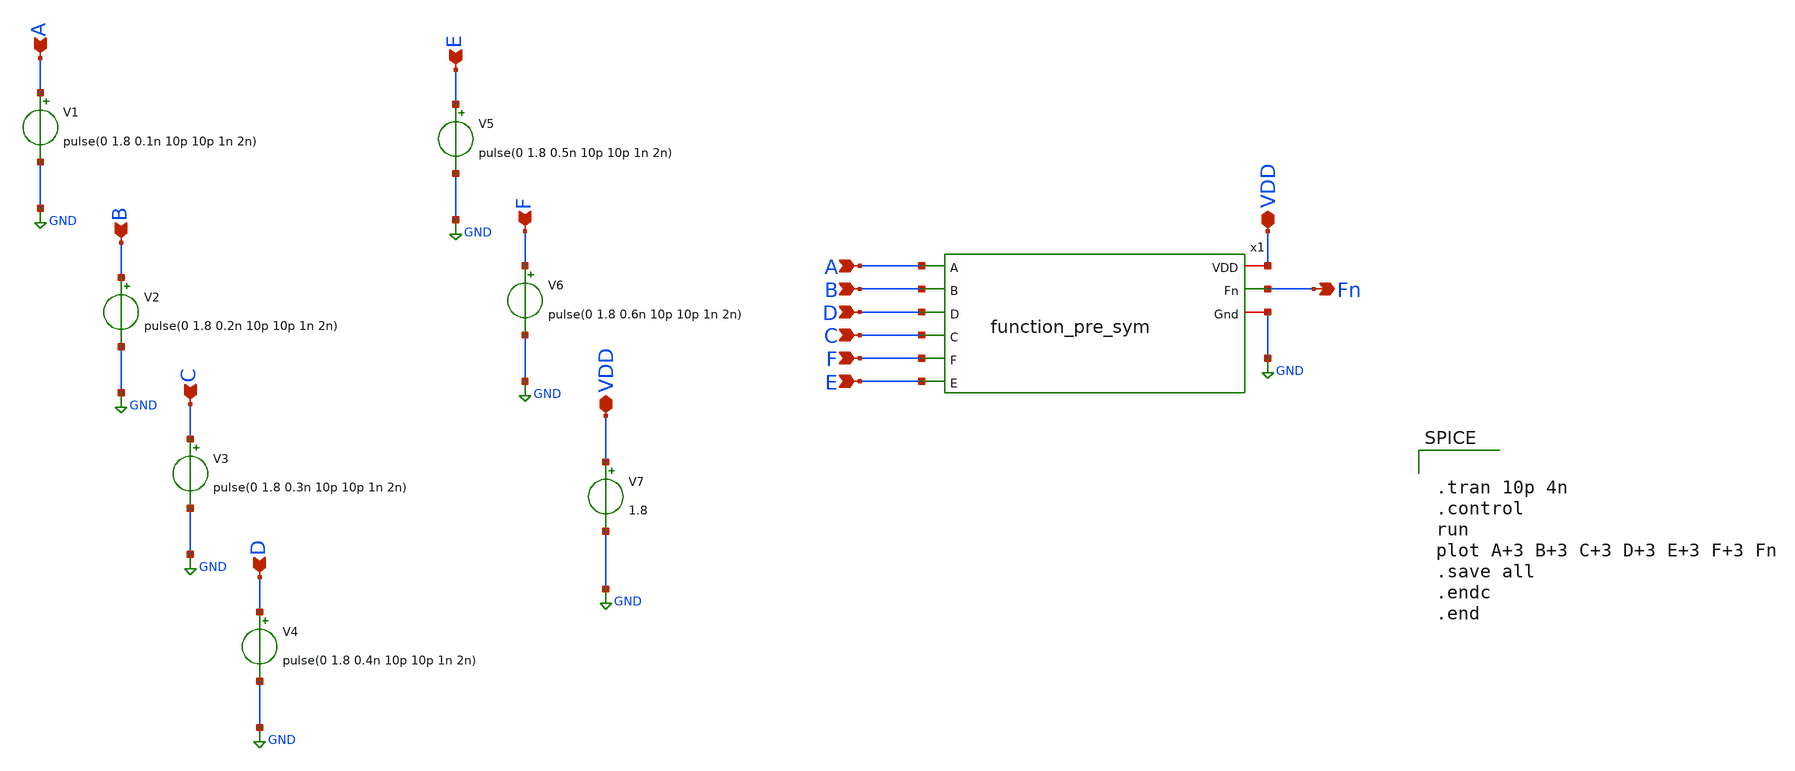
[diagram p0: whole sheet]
** sch_path: Week_1/Function_PreLayout/function_pre_tb.sch
**.subckt function_pre_tb A B C D E F E F C D B A VDD VDD Fn
*.ipin A
*.ipin B
*.ipin C
*.ipin D
*.ipin E
*.ipin F
*.ipin E
*.ipin F
*.ipin C
*.ipin D
*.ipin B
*.ipin A
*.iopin VDD
*.iopin VDD
*.opin Fn
V1 A GND pulse(0 1.8 0.1n 10p 10p 1n 2n)
V2 B GND pulse(0 1.8 0.2n 10p 10p 1n 2n)
V3 C GND pulse(0 1.8 0.3n 10p 10p 1n 2n)
V4 D GND pulse(0 1.8 0.4n 10p 10p 1n 2n)
V5 E GND pulse(0 1.8 0.5n 10p 10p 1n 2n)
V6 F GND pulse(0 1.8 0.6n 10p 10p 1n 2n)
V7 VDD GND 1.8
x1 VDD A B D C F E Fn GND function_pre_sym
**** begin user architecture code


.tran 10p 4n
.control
run
plot A+3 B+3 C+3 D+3 E+3 F+3 Fn
.save all
.endc
.end




.lib /home/swagatika/open_pdks/sky130/sky130A/libs.tech/ngspice/sky130.lib.spice tt

.save all



**** end user architecture code
**.ends

* expanding   symbol:  /home/swagatika/Desktop/Circuits/function_pre_sym.sym # of pins=9
** sym_path: Week_1/Function_PreLayout/function_pre_sym.sym
** sch_path: Week_1/Function_PreLayout/function_pre_sym.sch
.subckt function_pre_sym VDD A B D C F E Fn Gnd
*.ipin A
*.ipin B
*.ipin C
*.ipin D
*.ipin E
*.ipin F
*.opin Fn
*.iopin VDD
*.iopin Gnd
XM1 net3 A VDD VDD sky130_fd_pr__pfet_01v8 L=0.15 W=1 nf=1 ad='int((nf+1)/2) * W/nf * 0.29' as='int((nf+2)/2) * W/nf * 0.29'
+ pd='2*int((nf+1)/2) * (W/nf + 0.29)' ps='2*int((nf+2)/2) * (W/nf + 0.29)' nrd='0.29 / W' nrs='0.29 / W'
+ sa=0 sb=0 sd=0 mult=1 m=1
XM2 net1 B VDD VDD sky130_fd_pr__pfet_01v8 L=0.15 W=1 nf=1 ad='int((nf+1)/2) * W/nf * 0.29' as='int((nf+2)/2) * W/nf * 0.29'
+ pd='2*int((nf+1)/2) * (W/nf + 0.29)' ps='2*int((nf+2)/2) * (W/nf + 0.29)' nrd='0.29 / W' nrs='0.29 / W'
+ sa=0 sb=0 sd=0 mult=1 m=1
XM3 net2 C net3 net3 sky130_fd_pr__pfet_01v8 L=0.15 W=1 nf=1 ad='int((nf+1)/2) * W/nf * 0.29' as='int((nf+2)/2) * W/nf * 0.29'
+ pd='2*int((nf+1)/2) * (W/nf + 0.29)' ps='2*int((nf+2)/2) * (W/nf + 0.29)' nrd='0.29 / W' nrs='0.29 / W'
+ sa=0 sb=0 sd=0 mult=1 m=1
XM4 net2 D net1 net1 sky130_fd_pr__pfet_01v8 L=0.15 W=1 nf=1 ad='int((nf+1)/2) * W/nf * 0.29' as='int((nf+2)/2) * W/nf * 0.29'
+ pd='2*int((nf+1)/2) * (W/nf + 0.29)' ps='2*int((nf+2)/2) * (W/nf + 0.29)' nrd='0.29 / W' nrs='0.29 / W'
+ sa=0 sb=0 sd=0 mult=1 m=1
XM5 Fn E net2 net2 sky130_fd_pr__pfet_01v8 L=0.15 W=1 nf=1 ad='int((nf+1)/2) * W/nf * 0.29' as='int((nf+2)/2) * W/nf * 0.29'
+ pd='2*int((nf+1)/2) * (W/nf + 0.29)' ps='2*int((nf+2)/2) * (W/nf + 0.29)' nrd='0.29 / W' nrs='0.29 / W'
+ sa=0 sb=0 sd=0 mult=1 m=1
XM6 Fn F net2 net2 sky130_fd_pr__pfet_01v8 L=0.15 W=1 nf=1 ad='int((nf+1)/2) * W/nf * 0.29' as='int((nf+2)/2) * W/nf * 0.29'
+ pd='2*int((nf+1)/2) * (W/nf + 0.29)' ps='2*int((nf+2)/2) * (W/nf + 0.29)' nrd='0.29 / W' nrs='0.29 / W'
+ sa=0 sb=0 sd=0 mult=1 m=1
XM7 Fn A net4 net4 sky130_fd_pr__nfet_01v8 L=0.15 W=1 nf=1 ad='int((nf+1)/2) * W/nf * 0.29' as='int((nf+2)/2) * W/nf * 0.29'
+ pd='2*int((nf+1)/2) * (W/nf + 0.29)' ps='2*int((nf+2)/2) * (W/nf + 0.29)' nrd='0.29 / W' nrs='0.29 / W'
+ sa=0 sb=0 sd=0 mult=1 m=1
XM8 Fn C net4 net4 sky130_fd_pr__nfet_01v8 L=0.15 W=1 nf=1 ad='int((nf+1)/2) * W/nf * 0.29' as='int((nf+2)/2) * W/nf * 0.29'
+ pd='2*int((nf+1)/2) * (W/nf + 0.29)' ps='2*int((nf+2)/2) * (W/nf + 0.29)' nrd='0.29 / W' nrs='0.29 / W'
+ sa=0 sb=0 sd=0 mult=1 m=1
XM9 Fn E net5 net5 sky130_fd_pr__nfet_01v8 L=0.15 W=1 nf=1 ad='int((nf+1)/2) * W/nf * 0.29' as='int((nf+2)/2) * W/nf * 0.29'
+ pd='2*int((nf+1)/2) * (W/nf + 0.29)' ps='2*int((nf+2)/2) * (W/nf + 0.29)' nrd='0.29 / W' nrs='0.29 / W'
+ sa=0 sb=0 sd=0 mult=1 m=1
XM10 net4 B Gnd Gnd sky130_fd_pr__nfet_01v8 L=0.15 W=1 nf=1 ad='int((nf+1)/2) * W/nf * 0.29' as='int((nf+2)/2) * W/nf * 0.29'
+ pd='2*int((nf+1)/2) * (W/nf + 0.29)' ps='2*int((nf+2)/2) * (W/nf + 0.29)' nrd='0.29 / W' nrs='0.29 / W'
+ sa=0 sb=0 sd=0 mult=1 m=1
XM11 net4 D Gnd Gnd sky130_fd_pr__nfet_01v8 L=0.15 W=1 nf=1 ad='int((nf+1)/2) * W/nf * 0.29' as='int((nf+2)/2) * W/nf * 0.29'
+ pd='2*int((nf+1)/2) * (W/nf + 0.29)' ps='2*int((nf+2)/2) * (W/nf + 0.29)' nrd='0.29 / W' nrs='0.29 / W'
+ sa=0 sb=0 sd=0 mult=1 m=1
XM12 net5 F Gnd Gnd sky130_fd_pr__nfet_01v8 L=0.15 W=1 nf=1 ad='int((nf+1)/2) * W/nf * 0.29' as='int((nf+2)/2) * W/nf * 0.29'
+ pd='2*int((nf+1)/2) * (W/nf + 0.29)' ps='2*int((nf+2)/2) * (W/nf + 0.29)' nrd='0.29 / W' nrs='0.29 / W'
+ sa=0 sb=0 sd=0 mult=1 m=1
.ends

.GLOBAL GND
.end
